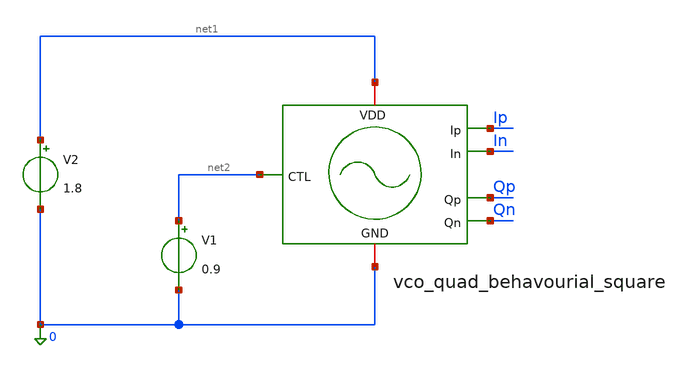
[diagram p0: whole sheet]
** sch_path: design/vco_2-4GHz/tests/vco_2-4GHz_behavourial_square_tb.sch
**.subckt vco_2-4GHz_behavourial_square_tb
V1 net2 0 0.9
V2 net1 0 1.8
**** begin user architecture code


.include xh018_ng/xh018.lib
.temp 30
.param vctl=0.9
.tran  0.1e-9 1e-6 uic


**** end user architecture code
**.ends
.end
